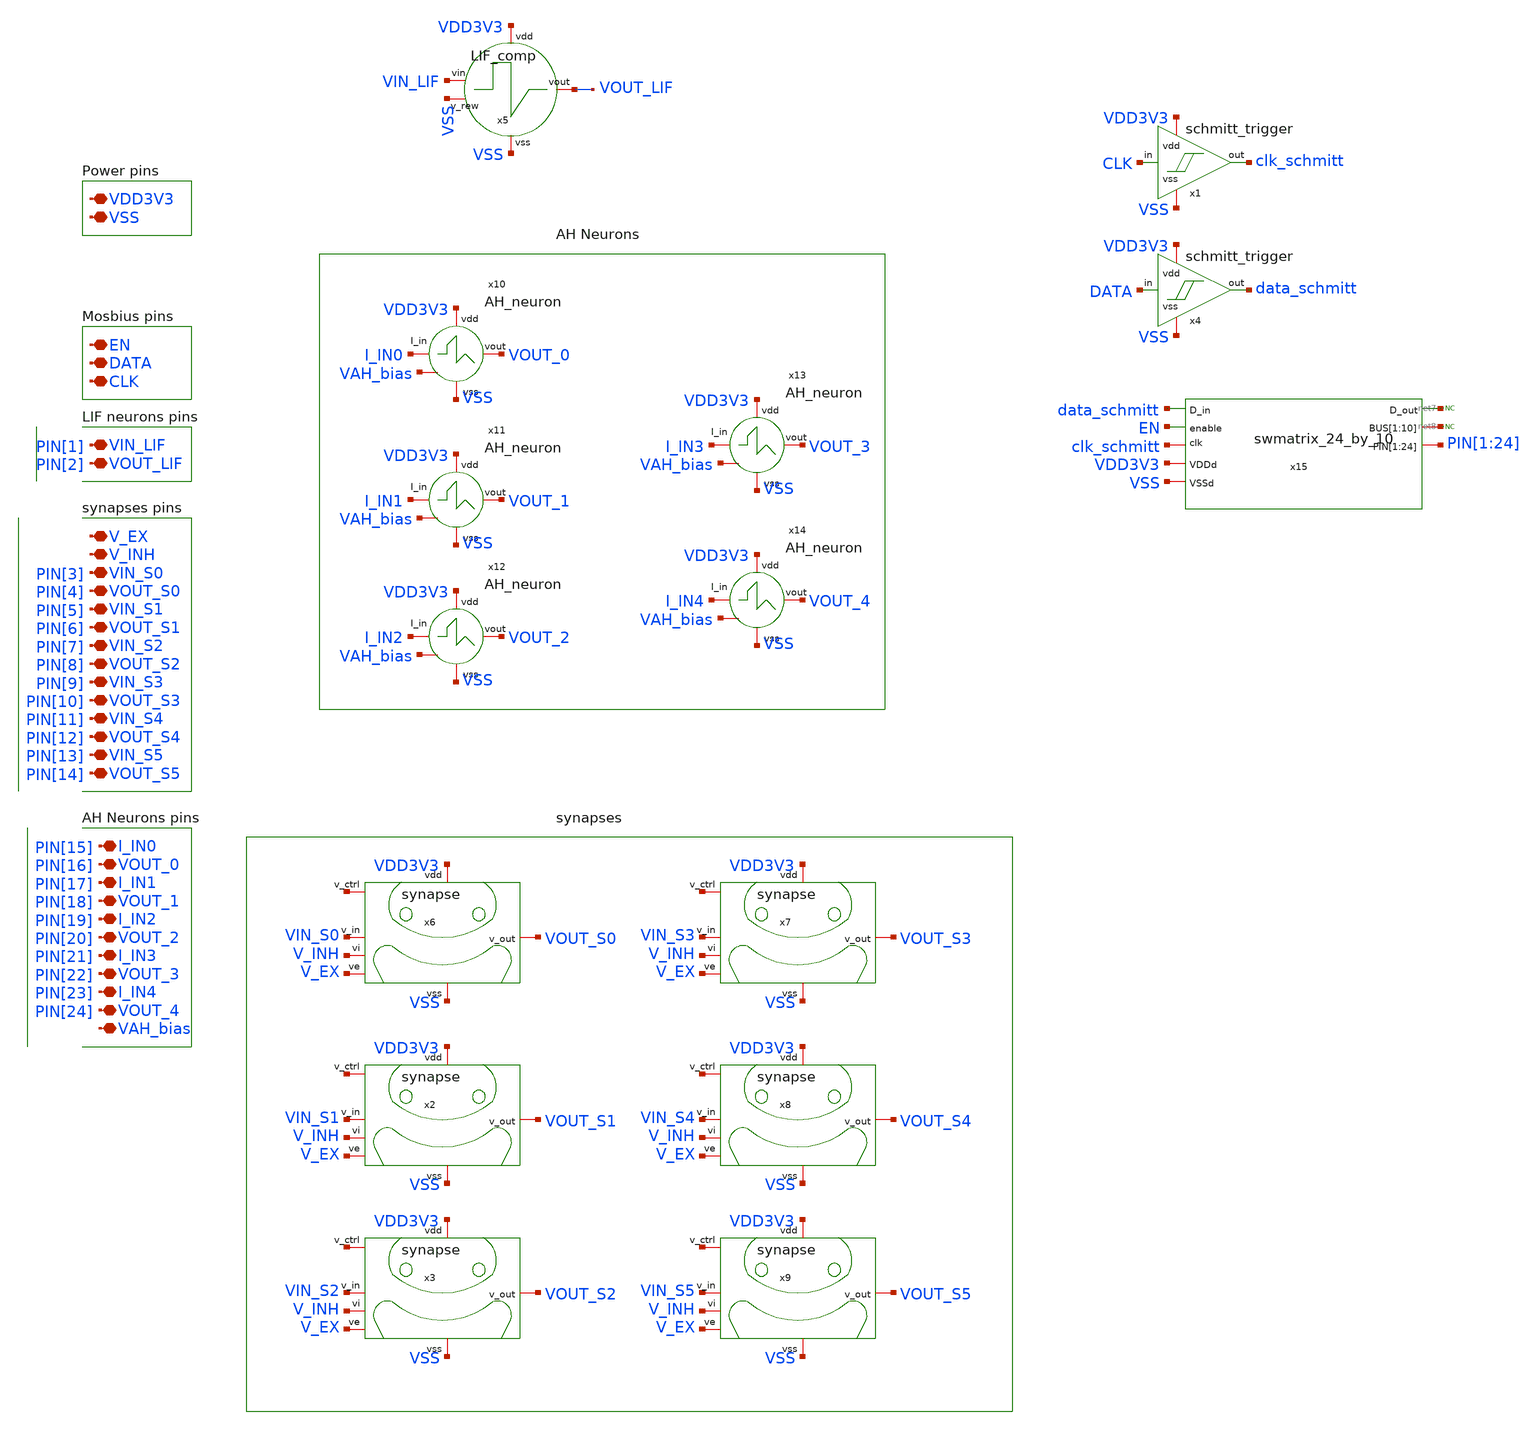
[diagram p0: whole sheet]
** sch_path: designs/klayout/layout_top/top.sch
**.subckt top I_IN0 VOUT_0 I_IN1 VOUT_1 I_IN2 VOUT_2 I_IN3 VOUT_3 VDD3V3 VSS VIN_LIF VOUT_LIF V_EX
*+ V_INH VIN_S0 VOUT_S0 VIN_S1 VOUT_S1 VIN_S2 VOUT_S2 EN DATA CLK I_IN4 VOUT_4 VIN_S3 VOUT_S3 VIN_S4 VOUT_S4
*+ VIN_S5 VOUT_S5 VAH_bias
*.iopin I_IN0
*.iopin VOUT_0
*.iopin I_IN1
*.iopin VOUT_1
*.iopin I_IN2
*.iopin VOUT_2
*.iopin I_IN3
*.iopin VOUT_3
*.iopin VDD3V3
*.iopin VSS
*.iopin VIN_LIF
*.iopin VOUT_LIF
*.iopin V_EX
*.iopin V_INH
*.iopin VIN_S0
*.iopin VOUT_S0
*.iopin VIN_S1
*.iopin VOUT_S1
*.iopin VIN_S2
*.iopin VOUT_S2
*.iopin EN
*.iopin DATA
*.iopin CLK
*.iopin I_IN4
*.iopin VOUT_4
*.iopin VIN_S3
*.iopin VOUT_S3
*.iopin VIN_S4
*.iopin VOUT_S4
*.iopin VIN_S5
*.iopin VOUT_S5
*.iopin VAH_bias
x5 VDD3V3 VSS VIN_LIF VSS VOUT_LIF LIF_comp
x6 VDD3V3 VIN_S0 V_EX net1 VOUT_S0 V_INH VSS synapse
x2 VDD3V3 VIN_S1 V_EX net2 VOUT_S1 V_INH VSS synapse
x3 VDD3V3 VIN_S2 V_EX net3 VOUT_S2 V_INH VSS synapse
x7 VDD3V3 VIN_S3 V_EX net4 VOUT_S3 V_INH VSS synapse
x8 VDD3V3 VIN_S4 V_EX net5 VOUT_S4 V_INH VSS synapse
x9 VDD3V3 VIN_S5 V_EX net6 VOUT_S5 V_INH VSS synapse
x10 VDD3V3 I_IN0 VOUT_0 VSS VAH_bias AH_neuron
x11 VDD3V3 I_IN1 VOUT_1 VSS VAH_bias AH_neuron
x12 VDD3V3 I_IN2 VOUT_2 VSS VAH_bias AH_neuron
x13 VDD3V3 I_IN3 VOUT_3 VSS VAH_bias AH_neuron
x14 VDD3V3 I_IN4 VOUT_4 VSS VAH_bias AH_neuron
x1 clk_schmitt CLK VDD3V3 VSS schmitt_trigger
x4 data_schmitt DATA VDD3V3 VSS schmitt_trigger
x15 net7 net8 net8 net8 net8 net8 net8 net8 net8 net8 net8 PIN[1] PIN[2] PIN[3] PIN[4] PIN[5] PIN[6]
+ PIN[7] PIN[8] PIN[9] PIN[10] PIN[11] PIN[12] PIN[13] PIN[14] PIN[15] PIN[16] PIN[17] PIN[18] PIN[19]
+ PIN[20] PIN[21] PIN[22] PIN[23] PIN[24] data_schmitt VDD3V3 EN VSS clk_schmitt swmatrix_24_by_10
* noconn #net7
* noconn #net8
**.ends
.end
